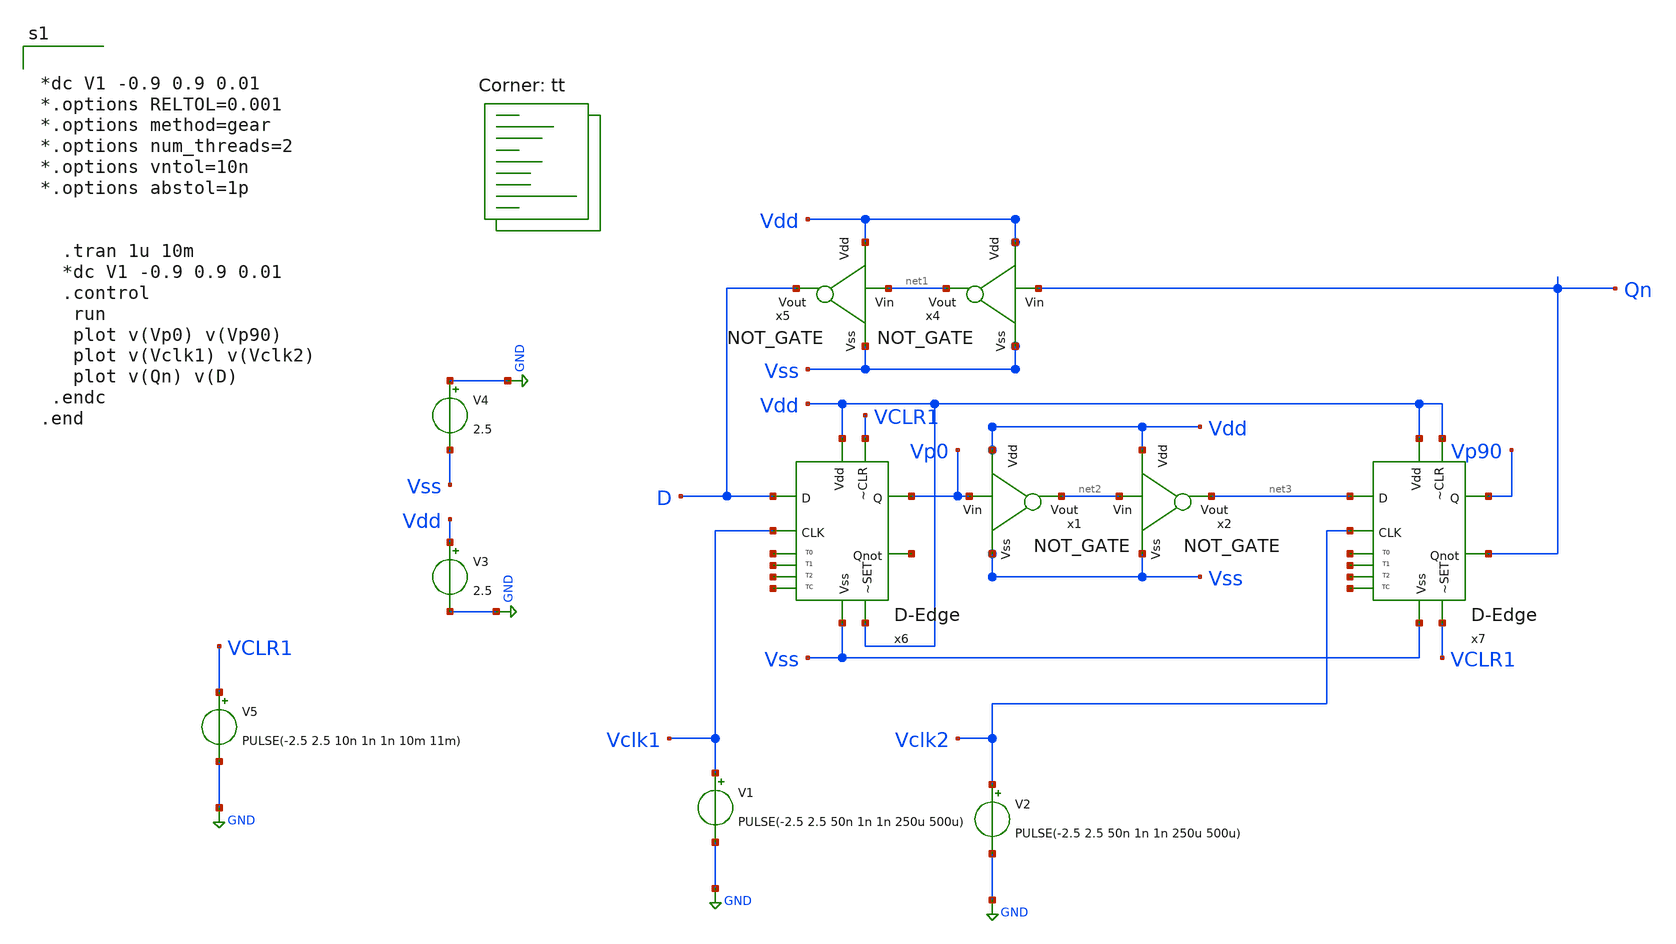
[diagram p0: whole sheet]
** sch_path: xschem/untitled-10.sch
**.subckt untitled-10
x6 Vdd Vss VCLR1 Vdd Vp0 D net4 Vclk1 net5 net6 net7 net8 D-Edge
x7 Vdd Vss Vdd VCLR1 Vp90 net3 Qn Vclk2 net9 net10 net11 net12 D-Edge
x4 Vdd net1 Qn Vss NOT_GATE
x5 Vdd D net1 Vss NOT_GATE
V1 Vclk1 GND PULSE(-2.5 2.5 50n 1n 1n 250u 500u)
V2 Vclk2 GND PULSE(-2.5 2.5 50n 1n 1n 250u 500u)
V4 GND Vss 2.5
V3 Vdd GND 2.5
V5 VCLR1 GND PULSE(-2.5 2.5 10n 1n 1n 10m 11m)
x1 Vdd net2 Vp0 Vss NOT_GATE
x2 Vdd net3 net2 Vss NOT_GATE
**** begin user architecture code
.lib $::SKYWATER_MODELS/sky130.lib.spice tt


*dc V1 -0.9 0.9 0.01
*.options RELTOL=0.001
*.options method=gear
*.options num_threads=2
*.options vntol=10n
*.options abstol=1p


  .tran 1u 10m
  *dc V1 -0.9 0.9 0.01
  .control
   run
   plot v(Vp0) v(Vp90)
   plot v(Vclk1) v(Vclk2)
   plot v(Qn) v(D)
 .endc
.end

**** end user architecture code
**.ends

* expanding   symbol:  D-Edge.sym # of pins=12
** sym_path: xschem/D-Edge.sym
** sch_path: xschem/D-Edge.sch
.subckt D-Edge Vdd Vss ~CLR ~SET Q D Qnot CLK TC T2 T1 T0
*.ipin D
*.ipin Vdd
*.ipin Vss
*.opin Q
*.opin Qnot
*.ipin ~CLR
*.ipin ~SET
*.ipin CLK
*.opin T0
*.opin T1
*.opin T2
*.opin TC
x1 CLK D T1 Vdd Vss CLK_I T-gate
x3 CLK_I T0 T1 Vdd Vss CLK T-gate
x4 CLK_I net1 T2 Vdd Vss CLK T-gate
x8 CLK Qnot T2 Vdd Vss CLK_I T-gate
x11 Vdd ~CLR T1 net1 Vss NAND_GATE
x2 Vdd ~SET net1 T0 Vss NAND_GATE
x5 Vdd ~CLR T2 Q Vss NAND_GATE
x7 Vdd ~SET Q Qnot Vss NAND_GATE
XM1 CLK_I CLK Vss Vss sky130_fd_pr__nfet_g5v0d10v5 L=1 W=3 nf=1 ad='int((1 + 1)/2) * 3 / 1 * 0.29' as='int((1 + 2)/2) * 3 / 1 * 0.29'
+ pd='2*int((1 + 1)/2) * (3 / 1 + 0.29)' ps='2*int((1 + 2)/2) * (3 / 1 + 0.29)' nrd='0.29 / 3 ' nrs='0.29 / 3 '
+ sa=0 sb=0 sd=0 mult=1 m=1
XM2 CLK_I CLK Vdd Vdd sky130_fd_pr__pfet_g5v0d10v5 L=1 W=27 nf=1 ad='int((1 + 1)/2) * 27 / 1 * 0.29'
+ as='int((1 + 2)/2) * 27 / 1 * 0.29' pd='2*int((1 + 1)/2) * (27 / 1 + 0.29)' ps='2*int((1 + 2)/2) * (27 / 1 + 0.29)'
+ nrd='0.29 / 27 ' nrs='0.29 / 27 ' sa=0 sb=0 sd=0 mult=1 m=1
XM3 TC CLK_I Vss Vss sky130_fd_pr__nfet_g5v0d10v5 L=1 W=3 nf=1 ad='int((1 + 1)/2) * 3 / 1 * 0.29' as='int((1 + 2)/2) * 3 / 1 * 0.29'
+ pd='2*int((1 + 1)/2) * (3 / 1 + 0.29)' ps='2*int((1 + 2)/2) * (3 / 1 + 0.29)' nrd='0.29 / 3 ' nrs='0.29 / 3 '
+ sa=0 sb=0 sd=0 mult=1 m=1
XM4 TC CLK_I Vdd Vdd sky130_fd_pr__pfet_g5v0d10v5 L=1 W=27 nf=1 ad='int((1 + 1)/2) * 27 / 1 * 0.29' as='int((1 + 2)/2) * 27 / 1 * 0.29'
+ pd='2*int((1 + 1)/2) * (27 / 1 + 0.29)' ps='2*int((1 + 2)/2) * (27 / 1 + 0.29)' nrd='0.29 / 27 ' nrs='0.29 / 27 '
+ sa=0 sb=0 sd=0 mult=1 m=1
.ends


* expanding   symbol:  NOT_GATE.sym # of pins=4
** sym_path: xschem/NOT_GATE.sym
** sch_path: xschem/NOT_GATE.sch
.subckt NOT_GATE Vdd Vout Vin Vss
*.opin Vout
*.ipin Vdd
*.ipin Vss
*.ipin Vin
XM1 Vout Vin Vss Vss sky130_fd_pr__nfet_g5v0d10v5 L=1 W=1 nf=1 ad='int((1 + 1)/2) * 1 / 1 * 0.29' as='int((1 + 2)/2) * 1 / 1 * 0.29'
+ pd='2*int((1 + 1)/2) * (1 / 1 + 0.29)' ps='2*int((1 + 2)/2) * (1 / 1 + 0.29)' nrd='0.29 / 1 ' nrs='0.29 / 1 '
+ sa=0 sb=0 sd=0 mult=1 m=1
XM2 Vout Vin Vdd Vdd sky130_fd_pr__pfet_g5v0d10v5 L=1 W=3 nf=1 ad='int((1 + 1)/2) * 3 / 1 * 0.29' as='int((1 + 2)/2) * 3 / 1 * 0.29'
+ pd='2*int((1 + 1)/2) * (3 / 1 + 0.29)' ps='2*int((1 + 2)/2) * (3 / 1 + 0.29)' nrd='0.29 / 3 ' nrs='0.29 / 3 '
+ sa=0 sb=0 sd=0 mult=1 m=1
.ends


* expanding   symbol:  T-gate.sym # of pins=6
** sym_path: xschem/T-gate.sym
** sch_path: xschem/T-gate.sch
.subckt T-gate I_CLK T_In T_Out Vdd Vss CLK
*.ipin T_In
*.opin T_Out
*.ipin Vdd
*.ipin Vss
*.ipin I_CLK
*.ipin CLK
XM1 T_In I_CLK T_Out Vdd sky130_fd_pr__pfet_g5v0d10v5 L=0.5 W=3 nf=1 ad='int((1 + 1)/2) * 3 / 1 * 0.29'
+ as='int((1 + 2)/2) * 3 / 1 * 0.29' pd='2*int((1 + 1)/2) * (3 / 1 + 0.29)' ps='2*int((1 + 2)/2) * (3 / 1 + 0.29)'
+ nrd='0.29 / 3 ' nrs='0.29 / 3 ' sa=0 sb=0 sd=0 mult=1 m=1
XM3 T_Out CLK T_In Vss sky130_fd_pr__nfet_g5v0d10v5 L=0.5 W=1 nf=1 ad='int((1 + 1)/2) * 1 / 1 * 0.29'
+ as='int((1 + 2)/2) * 1 / 1 * 0.29' pd='2*int((1 + 1)/2) * (1 / 1 + 0.29)' ps='2*int((1 + 2)/2) * (1 / 1 + 0.29)'
+ nrd='0.29 / 1 ' nrs='0.29 / 1 ' sa=0 sb=0 sd=0 mult=1 m=1
XM2 T_Out CLK T_Out Vdd sky130_fd_pr__pfet_g5v0d10v5 L=0.5 W=1.5 nf=1 ad='int((1 + 1)/2) * 1.5 / 1 * 0.29'
+ as='int((1 + 2)/2) * 1.5 / 1 * 0.29' pd='2*int((1 + 1)/2) * (1.5 / 1 + 0.29)' ps='2*int((1 + 2)/2) * (1.5 / 1 + 0.29)'
+ nrd='0.29 / 1.5 ' nrs='0.29 / 1.5 ' sa=0 sb=0 sd=0 mult=1 m=1
XM4 T_In CLK T_In Vdd sky130_fd_pr__pfet_g5v0d10v5 L=0.5 W=1.5 nf=1 ad='int((1 + 1)/2) * 1.5 / 1 * 0.29'
+ as='int((1 + 2)/2) * 1.5 / 1 * 0.29' pd='2*int((1 + 1)/2) * (1.5 / 1 + 0.29)' ps='2*int((1 + 2)/2) * (1.5 / 1 + 0.29)'
+ nrd='0.29 / 1.5 ' nrs='0.29 / 1.5 ' sa=0 sb=0 sd=0 mult=1 m=1
XM5 T_In I_CLK T_In Vss sky130_fd_pr__nfet_g5v0d10v5 L=0.5 W=0.5 nf=1 ad='int((1 + 1)/2) * 0.5 / 1 * 0.29'
+ as='int((1 + 2)/2) * 0.5 / 1 * 0.29' pd='2*int((1 + 1)/2) * (0.5 / 1 + 0.29)' ps='2*int((1 + 2)/2) * (0.5 / 1 + 0.29)'
+ nrd='0.29 / 0.5 ' nrs='0.29 / 0.5 ' sa=0 sb=0 sd=0 mult=1 m=1
XM6 T_Out I_CLK T_Out Vss sky130_fd_pr__nfet_g5v0d10v5 L=0.5 W=0.5 nf=1 ad='int((1 + 1)/2) * 0.5 / 1 * 0.29'
+ as='int((1 + 2)/2) * 0.5 / 1 * 0.29' pd='2*int((1 + 1)/2) * (0.5 / 1 + 0.29)' ps='2*int((1 + 2)/2) * (0.5 / 1 + 0.29)'
+ nrd='0.29 / 0.5 ' nrs='0.29 / 0.5 ' sa=0 sb=0 sd=0 mult=1 m=1
.ends


* expanding   symbol:  NAND_GATE.sym # of pins=5
** sym_path: xschem/NAND_GATE.sym
** sch_path: xschem/NAND_GATE.sch
.subckt NAND_GATE Vdd A B Vout Vss
*.ipin Vdd
*.ipin Vss
*.ipin A
*.ipin B
*.opin Vout
XM3 Vout A net1 Vss sky130_fd_pr__nfet_g5v0d10v5 L=0.5 W=1 nf=1 ad='int((1 + 1)/2) * 1 / 1 * 0.29' as='int((1 + 2)/2) * 1 / 1 * 0.29'
+ pd='2*int((1 + 1)/2) * (1 / 1 + 0.29)' ps='2*int((1 + 2)/2) * (1 / 1 + 0.29)' nrd='0.29 / 1 ' nrs='0.29 / 1 '
+ sa=0 sb=0 sd=0 mult=1 m=1
XM4 Vout A Vdd Vdd sky130_fd_pr__pfet_g5v0d10v5 L=0.5 W=3 nf=1 ad='int((1 + 1)/2) * 3 / 1 * 0.29' as='int((1 + 2)/2) * 3 / 1 * 0.29'
+ pd='2*int((1 + 1)/2) * (3 / 1 + 0.29)' ps='2*int((1 + 2)/2) * (3 / 1 + 0.29)' nrd='0.29 / 3 ' nrs='0.29 / 3 '
+ sa=0 sb=0 sd=0 mult=1 m=1
XM5 Vout B Vdd Vdd sky130_fd_pr__pfet_g5v0d10v5 L=0.5 W=3 nf=1 ad='int((1 + 1)/2) * 3 / 1 * 0.29' as='int((1 + 2)/2) * 3 / 1 * 0.29'
+ pd='2*int((1 + 1)/2) * (3 / 1 + 0.29)' ps='2*int((1 + 2)/2) * (3 / 1 + 0.29)' nrd='0.29 / 3 ' nrs='0.29 / 3 '
+ sa=0 sb=0 sd=0 mult=1 m=1
XM1 net1 B Vss Vss sky130_fd_pr__nfet_g5v0d10v5 L=0.5 W=1 nf=1 ad='int((1 + 1)/2) * 1 / 1 * 0.29' as='int((1 + 2)/2) * 1 / 1 * 0.29'
+ pd='2*int((1 + 1)/2) * (1 / 1 + 0.29)' ps='2*int((1 + 2)/2) * (1 / 1 + 0.29)' nrd='0.29 / 1 ' nrs='0.29 / 1 '
+ sa=0 sb=0 sd=0 mult=1 m=1
.ends

.GLOBAL GND
.end
